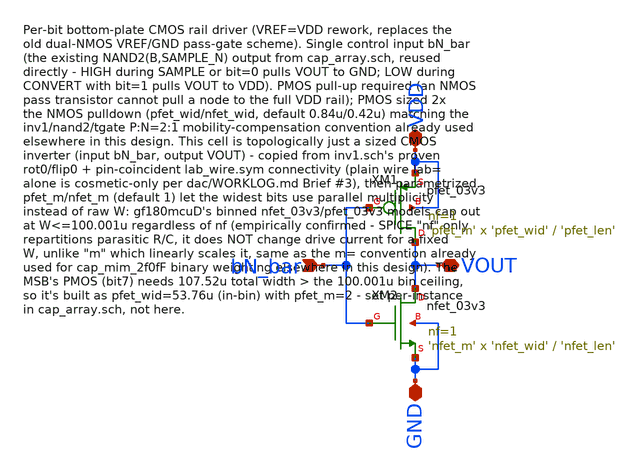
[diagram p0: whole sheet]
** sch_path: dac/schematic/unit_switch.sch
**.subckt unit_switch bN_bar VOUT VDD GND
*.ipin bN_bar
*.iopin VOUT
*.iopin VDD
*.iopin GND
XM1 VOUT bN_bar VDD VDD pfet_03v3 L='pfet_len' W='pfet_wid' nf=1 ad='int((nf+1)/2) * W/nf * 0.18u' as='int((nf+2)/2) * W/nf * 0.18u'
+ pd='2*int((nf+1)/2) * (W/nf + 0.18u)' ps='2*int((nf+2)/2) * (W/nf + 0.18u)' nrd='0.18u / W' nrs='0.18u / W'
+ sa=0 sb=0 sd=0 m='pfet_m'
XM2 VOUT bN_bar GND GND nfet_03v3 L='nfet_len' W='nfet_wid' nf=1 ad='int((nf+1)/2) * W/nf * 0.18u' as='int((nf+2)/2) * W/nf * 0.18u'
+ pd='2*int((nf+1)/2) * (W/nf + 0.18u)' ps='2*int((nf+2)/2) * (W/nf + 0.18u)' nrd='0.18u / W' nrs='0.18u / W'
+ sa=0 sb=0 sd=0 m='nfet_m'
**.ends
.end
